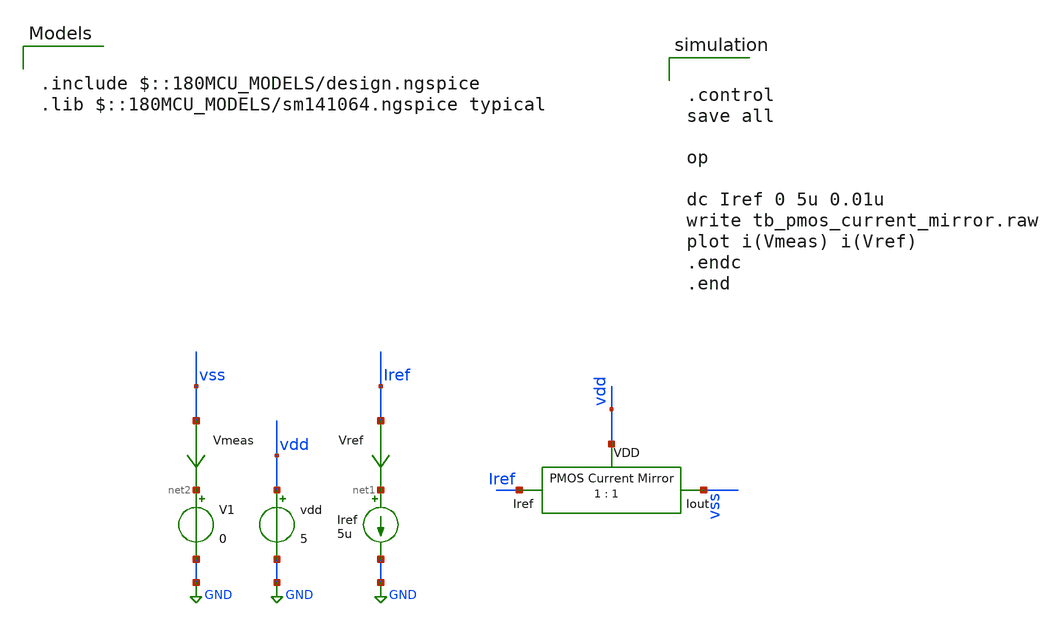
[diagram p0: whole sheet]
** sch_path: designs/libs/tb_analog/tb_pmos_current_mirror/tb_pmos_current_mirror.sch
**.subckt tb_pmos_current_mirror
Iref net1 GND 5u
vdd vdd GND 5
V1 net2 GND 0
Vmeas vss net2 0
.save i(vmeas)
Vref Iref net1 0
.save i(vref)
x1 vdd vss Iref pmos_current_mirror
**** begin user architecture code


.control
save all

op

dc Iref 0 5u 0.01u
write tb_pmos_current_mirror.raw
plot i(Vmeas) i(Vref)
.endc
.end



.include $::180MCU_MODELS/design.ngspice
.lib $::180MCU_MODELS/sm141064.ngspice typical

**** end user architecture code
**.ends

* expanding   symbol:  libs/core_analog/current-mirror/pmos_current_mirror.sym # of pins=3
** sym_path: designs/libs/core_analog/current-mirror/pmos_current_mirror.sym
** sch_path: designs/libs/core_analog/current-mirror/pmos_current_mirror.sch
.subckt pmos_current_mirror VDD Iout Iref
*.ipin VDD
*.ipin Iref
*.opin Iout
XM2 net2 net1 VDD VDD pfet_05v0 L=0.50u W=0.30u nf=1 ad='int((nf+1)/2) * W/nf * 0.18u' as='int((nf+2)/2) * W/nf * 0.18u'
+ pd='2*int((nf+1)/2) * (W/nf + 0.18u)' ps='2*int((nf+2)/2) * (W/nf + 0.18u)' nrd='0.18u / W' nrs='0.18u / W'
+ sa=0 sb=0 sd=0 m=1
XM1 net1 net1 VDD VDD pfet_05v0 L=0.50u W=0.30u nf=1 ad='int((nf+1)/2) * W/nf * 0.18u' as='int((nf+2)/2) * W/nf * 0.18u'
+ pd='2*int((nf+1)/2) * (W/nf + 0.18u)' ps='2*int((nf+2)/2) * (W/nf + 0.18u)' nrd='0.18u / W' nrs='0.18u / W'
+ sa=0 sb=0 sd=0 m=1
XM3 Iout Iref net2 net2 pfet_05v0 L=0.50u W=0.30u nf=1 ad='int((nf+1)/2) * W/nf * 0.18u' as='int((nf+2)/2) * W/nf * 0.18u'
+ pd='2*int((nf+1)/2) * (W/nf + 0.18u)' ps='2*int((nf+2)/2) * (W/nf + 0.18u)' nrd='0.18u / W' nrs='0.18u / W'
+ sa=0 sb=0 sd=0 m=1
XM4 Iref Iref net1 net1 pfet_05v0 L=0.50u W=0.30u nf=1 ad='int((nf+1)/2) * W/nf * 0.18u' as='int((nf+2)/2) * W/nf * 0.18u'
+ pd='2*int((nf+1)/2) * (W/nf + 0.18u)' ps='2*int((nf+2)/2) * (W/nf + 0.18u)' nrd='0.18u / W' nrs='0.18u / W'
+ sa=0 sb=0 sd=0 m=1
.ends

.GLOBAL GND
.end
